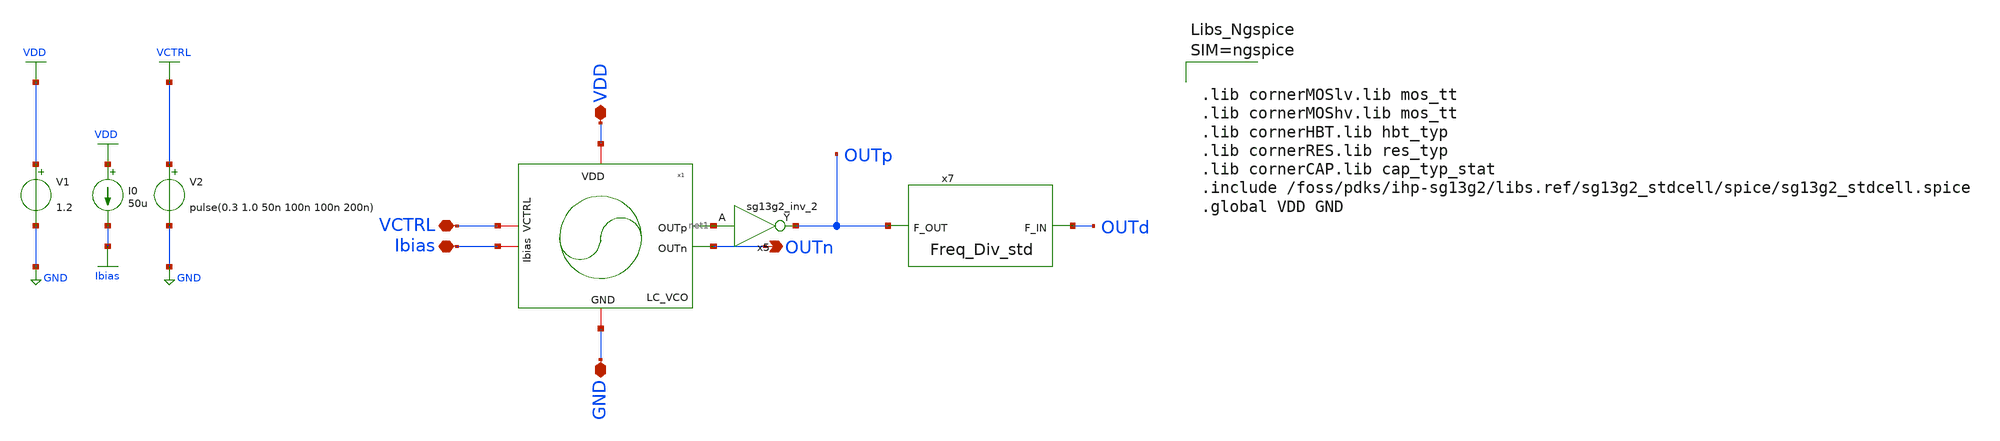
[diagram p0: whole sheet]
** sch_path: schematic/Test/LCVCO_temp_Fredivider_tb.sch
**.subckt LCVCO_temp_Fredivider_tb OUTn VDD VCTRL GND Ibias
*.opin OUTn
*.iopin VDD
*.iopin VCTRL
*.iopin GND
*.iopin Ibias
x5 OUTp net1 VDD GND sg13g2_inv_2
V1 VDD GND 1.2
V2 VCTRL GND pulse(0.3 1.0 50n 100n 100n 200n)
I0 VDD Ibias 50u
x4 VDD net1 OUTn Ibias VCTRL GND LC_VCO
x7 OUTd OUTp Freq_Div_std
**** begin user architecture code



.model freq_div freq_div
.include ./IHP_4nH_Inductor.spice
.param temp=27
.control
pre_osdi ./freq_div.osdi
save all
*.ic v(OUTp)=0.6

tran 1p 40n UIC

linearize v(OUTp) v(Vctrl) v(outd)

    let n_pts = length(time)
    let freq_vector = unitvec(n_pts) * 0

    * Advanced script to calculate instantaneous frequency
    let i = 1
    let last_cross = 0
    while i < length(time)
        if (v(OUTp)[i] >= 0.6) & (v(OUTp)[i-1] < 0.6)
            let current_cross = time[i]
            let period = current_cross - last_cross
            let inst_freq = 1 / period
            let freq_vector[i] = inst_freq
            let last_cross = current_cross
        else
            let freq_vector[i] = freq_vector[i-1]
        end
        let i = i + 1
    end

* Save transient waveform to raw file
write LCVCO_freqdiv.raw

*quit 0
.endc






.lib cornerMOSlv.lib mos_tt
.lib cornerMOShv.lib mos_tt
.lib cornerHBT.lib hbt_typ
.lib cornerRES.lib res_typ
.lib cornerCAP.lib cap_typ_stat
.include /foss/pdks/ihp-sg13g2/libs.ref/sg13g2_stdcell/spice/sg13g2_stdcell.spice
.global VDD GND




**** end user architecture code
**.ends
.GLOBAL GND
.GLOBAL VDD
.GLOBAL VCTRL
.GLOBAL Ibias
.end
